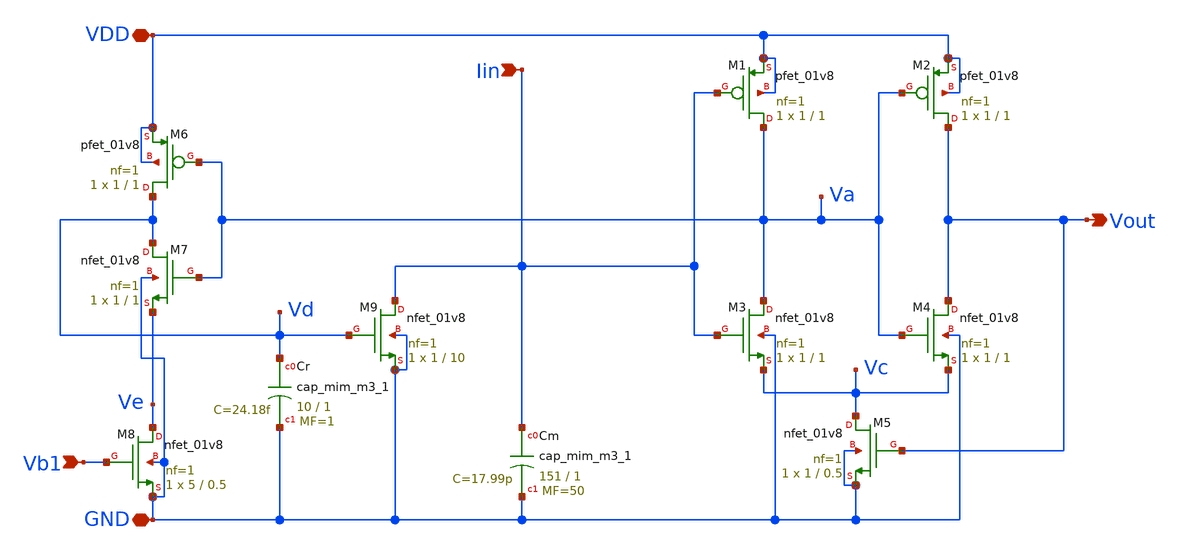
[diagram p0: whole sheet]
** sch_path: LIF_neuron/LIF_neuron_Vohra_CC.sch
**.subckt LIF_neuron_Vohra_CC GND Vb1 VDD Vout Iin
*.iopin GND
*.ipin Vb1
*.iopin VDD
*.opin Vout
*.ipin Iin
XM8 Ve Vb1 GND GND sky130_fd_pr__nfet_01v8 L=0.5 W=5 nf=1 ad='int((nf+1)/2) * W/nf * 0.29' as='int((nf+2)/2) * W/nf * 0.29'
+ pd='2*int((nf+1)/2) * (W/nf + 0.29)' ps='2*int((nf+2)/2) * (W/nf + 0.29)' nrd='0.29 / W' nrs='0.29 / W'
+ sa=0 sb=0 sd=0 mult=1 m=1
XM7 Vd Va Ve GND sky130_fd_pr__nfet_01v8 L=1 W=1 nf=1 ad='int((nf+1)/2) * W/nf * 0.29' as='int((nf+2)/2) * W/nf * 0.29'
+ pd='2*int((nf+1)/2) * (W/nf + 0.29)' ps='2*int((nf+2)/2) * (W/nf + 0.29)' nrd='0.29 / W' nrs='0.29 / W'
+ sa=0 sb=0 sd=0 mult=1 m=1
XM6 Vd Va VDD VDD sky130_fd_pr__pfet_01v8 L=1 W=1 nf=1 ad='int((nf+1)/2) * W/nf * 0.29' as='int((nf+2)/2) * W/nf * 0.29'
+ pd='2*int((nf+1)/2) * (W/nf + 0.29)' ps='2*int((nf+2)/2) * (W/nf + 0.29)' nrd='0.29 / W' nrs='0.29 / W'
+ sa=0 sb=0 sd=0 mult=1 m=1
XCr Vd GND sky130_fd_pr__cap_mim_m3_1 W=10 L=1 MF=1 m=1
XM9 Iin Vd GND GND sky130_fd_pr__nfet_01v8 L=10 W=1 nf=1 ad='int((nf+1)/2) * W/nf * 0.29' as='int((nf+2)/2) * W/nf * 0.29'
+ pd='2*int((nf+1)/2) * (W/nf + 0.29)' ps='2*int((nf+2)/2) * (W/nf + 0.29)' nrd='0.29 / W' nrs='0.29 / W'
+ sa=0 sb=0 sd=0 mult=1 m=1
XCm Iin GND sky130_fd_pr__cap_mim_m3_1 W=151 L=1 MF=50 m=50
XM5 Vc Vout GND GND sky130_fd_pr__nfet_01v8 L=0.5 W=1 nf=1 ad='int((nf+1)/2) * W/nf * 0.29' as='int((nf+2)/2) * W/nf * 0.29'
+ pd='2*int((nf+1)/2) * (W/nf + 0.29)' ps='2*int((nf+2)/2) * (W/nf + 0.29)' nrd='0.29 / W' nrs='0.29 / W'
+ sa=0 sb=0 sd=0 mult=1 m=1
XM3 Va Iin Vc GND sky130_fd_pr__nfet_01v8 L=1 W=1 nf=1 ad='int((nf+1)/2) * W/nf * 0.29' as='int((nf+2)/2) * W/nf * 0.29'
+ pd='2*int((nf+1)/2) * (W/nf + 0.29)' ps='2*int((nf+2)/2) * (W/nf + 0.29)' nrd='0.29 / W' nrs='0.29 / W'
+ sa=0 sb=0 sd=0 mult=1 m=1
XM1 Va Iin VDD VDD sky130_fd_pr__pfet_01v8 L=1 W=1 nf=1 ad='int((nf+1)/2) * W/nf * 0.29' as='int((nf+2)/2) * W/nf * 0.29'
+ pd='2*int((nf+1)/2) * (W/nf + 0.29)' ps='2*int((nf+2)/2) * (W/nf + 0.29)' nrd='0.29 / W' nrs='0.29 / W'
+ sa=0 sb=0 sd=0 mult=1 m=1
XM4 Vout Va Vc GND sky130_fd_pr__nfet_01v8 L=1 W=1 nf=1 ad='int((nf+1)/2) * W/nf * 0.29' as='int((nf+2)/2) * W/nf * 0.29'
+ pd='2*int((nf+1)/2) * (W/nf + 0.29)' ps='2*int((nf+2)/2) * (W/nf + 0.29)' nrd='0.29 / W' nrs='0.29 / W'
+ sa=0 sb=0 sd=0 mult=1 m=1
XM2 Vout Va VDD VDD sky130_fd_pr__pfet_01v8 L=1 W=1 nf=1 ad='int((nf+1)/2) * W/nf * 0.29' as='int((nf+2)/2) * W/nf * 0.29'
+ pd='2*int((nf+1)/2) * (W/nf + 0.29)' ps='2*int((nf+2)/2) * (W/nf + 0.29)' nrd='0.29 / W' nrs='0.29 / W'
+ sa=0 sb=0 sd=0 mult=1 m=1
**.ends
.end
